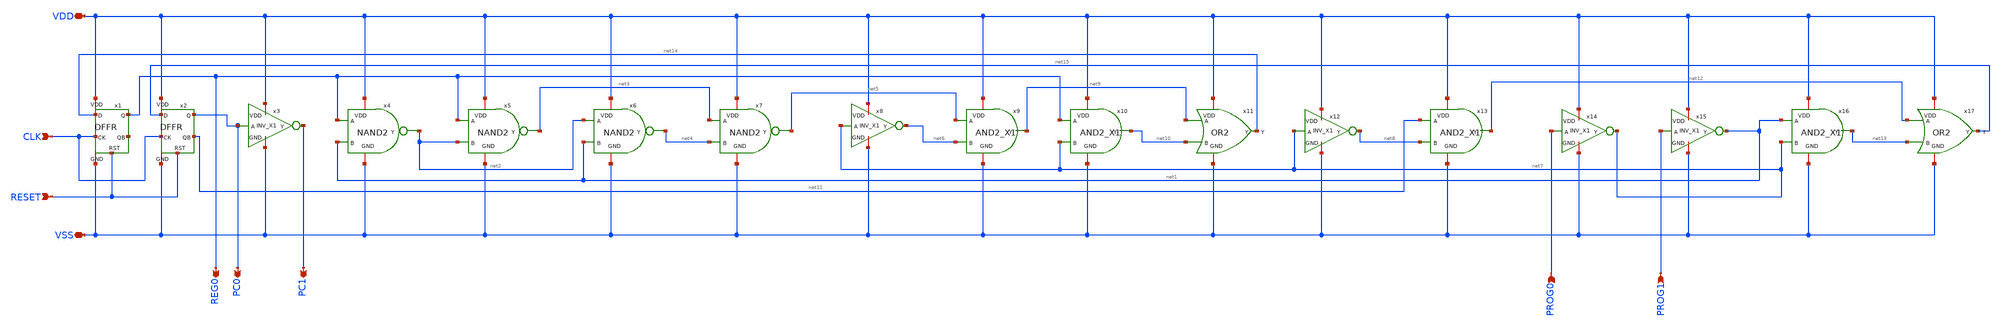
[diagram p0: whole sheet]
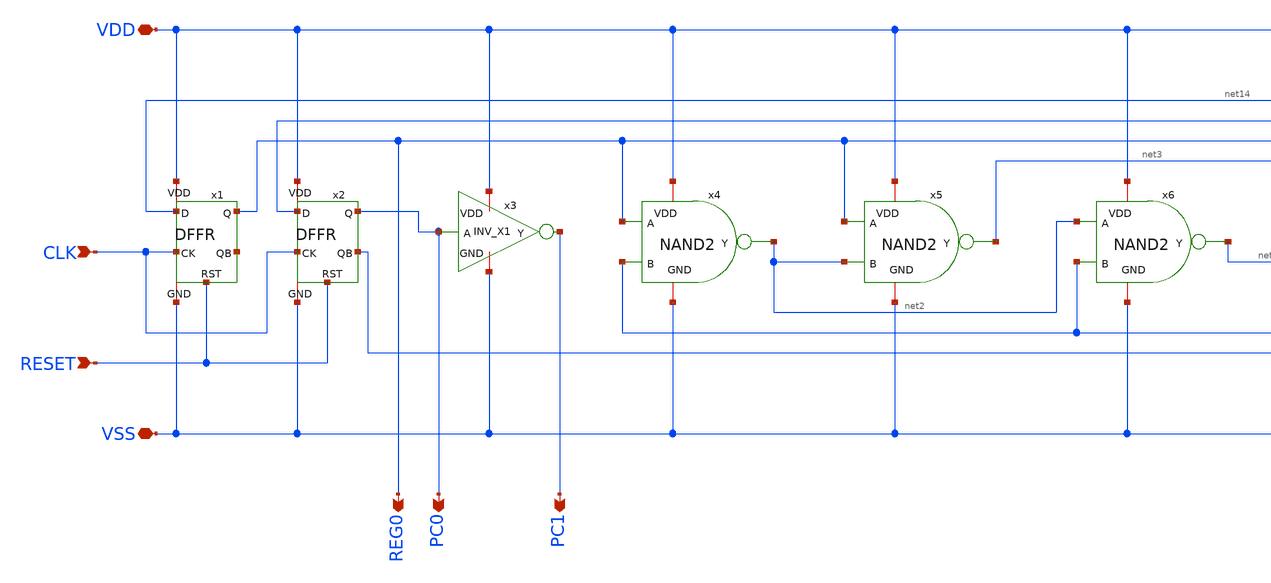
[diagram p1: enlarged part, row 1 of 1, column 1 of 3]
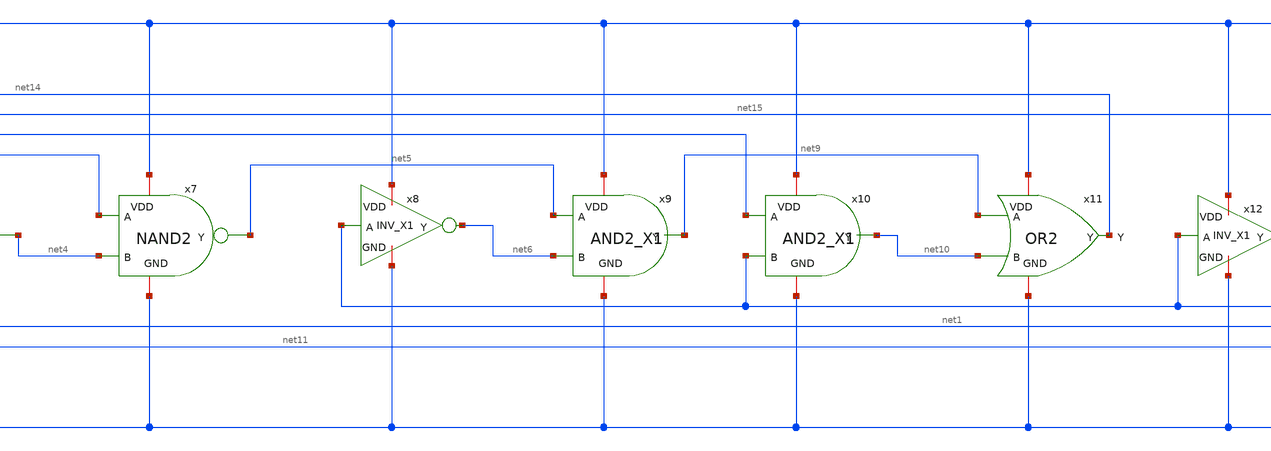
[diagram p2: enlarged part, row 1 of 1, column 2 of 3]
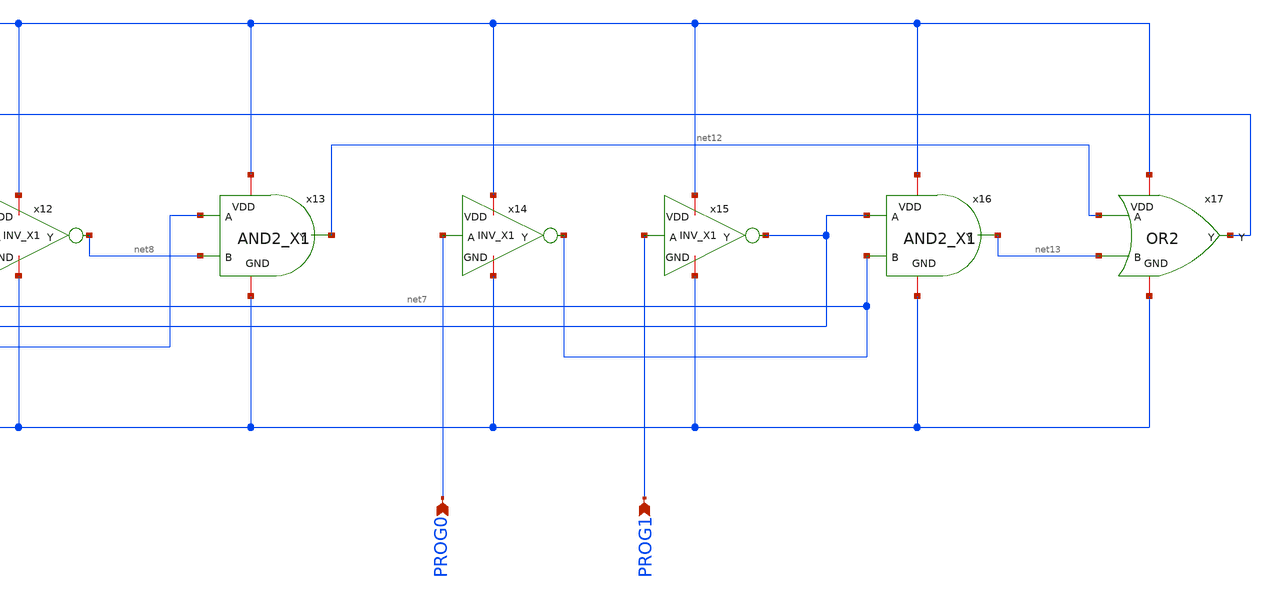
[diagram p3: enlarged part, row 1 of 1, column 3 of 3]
** sch_path: member_project/1bit-CPU_ALL/1bit-CPU_MUX_kyushu/1bit-CPU_1line_sadakata.sch
**.subckt 1bit-CPU_1line_sadakata VDD VSS CLK RESET REG0 PROG1 PROG0 PC0 PC1
*.iopin VDD
*.iopin VSS
*.ipin CLK
*.ipin RESET
*.opin REG0
*.ipin PROG1
*.ipin PROG0
*.opin PC0
*.opin PC1
x1 VDD net16 net14 REG0 RESET VSS CLK DFFR
x2 VDD net11 net15 PC0 RESET VSS CLK DFFR
x3 VDD PC0 PC1 VSS INV_X1
x4 VDD net2 REG0 net1 VSS NAND2
x5 VDD net3 REG0 net2 VSS NAND2
x6 VDD net4 net2 net1 VSS NAND2
x7 VDD net5 net3 net4 VSS NAND2
x8 VDD net7 net6 VSS INV_X1
x9 VDD net9 net5 net6 VSS AND2_X1
x10 VDD net10 REG0 net7 VSS AND2_X1
x11 VDD net14 net9 net10 VSS OR2
x12 VDD net7 net8 VSS INV_X1
x13 VDD net12 net11 net8 VSS AND2_X1
x14 VDD PROG0 net7 VSS INV_X1
x15 VDD PROG1 net1 VSS INV_X1
x16 VDD net13 net1 net7 VSS AND2_X1
x17 VDD net15 net12 net13 VSS OR2
**.ends

* expanding   symbol:  IP62_5_stdcell/DFFR.sym # of pins=7
** sym_path: IP62_5_stdcell/DFFR.sym
** sch_path: IP62_5_stdcell/DFFR.sch
.subckt DFFR VDD QB D Q RST GND CK
*.iopin VDD
*.iopin GND
*.ipin CK
*.ipin D
*.opin Q
*.opin QB
*.ipin RST
XM2 net2 D VDD VDD PMOS w=10.2u l=1u as=0 ad=0 ps=0 pd=0 nrd=0 nrs=0 m=1
XM1 net3 CLK net2 VDD PMOS w=10.2u l=1u as=0 ad=0 ps=0 pd=0 nrd=0 nrs=0 m=1
XM11 net5 net8 VDD VDD PMOS w=10.2u l=1u as=0 ad=0 ps=0 pd=0 nrd=0 nrs=0 m=1
XM12 net3 CKB net5 VDD PMOS w=10.2u l=1u as=0 ad=0 ps=0 pd=0 nrd=0 nrs=0 m=1
XM15 net7 net3 VDD VDD PMOS w=10.2u l=1u as=0 ad=0 ps=0 pd=0 nrd=0 nrs=0 m=1
XM16 net8 RST net7 VDD PMOS w=10.2u l=1u as=0 ad=0 ps=0 pd=0 nrd=0 nrs=0 m=1
XM18 net9 net8 VDD VDD PMOS w=10.2u l=1u as=0 ad=0 ps=0 pd=0 nrd=0 nrs=0 m=1
XM19 net10 CKB net9 VDD PMOS w=10.2u l=1u as=0 ad=0 ps=0 pd=0 nrd=0 nrs=0 m=1
XM23 net12 net14 VDD VDD PMOS w=10.2u l=1u as=0 ad=0 ps=0 pd=0 nrd=0 nrs=0 m=1
XM24 net10 CLK net12 VDD PMOS w=10.2u l=1u as=0 ad=0 ps=0 pd=0 nrd=0 nrs=0 m=1
XM27 net15 net10 VDD VDD PMOS w=10.2u l=1u as=0 ad=0 ps=0 pd=0 nrd=0 nrs=0 m=1
XM28 net14 RST net15 VDD PMOS w=10.2u l=1u as=0 ad=0 ps=0 pd=0 nrd=0 nrs=0 m=1
XM31 QB net14 VDD VDD PMOS w=10.2u l=1u as=0 ad=0 ps=0 pd=0 nrd=0 nrs=0 m=1
XM33 Q QB VDD VDD PMOS w=10.2u l=1u as=0 ad=0 ps=0 pd=0 nrd=0 nrs=0 m=1
XM35 QB net14 GND GND NMOS w=3.4u l=1u as=0 ad=0 ps=0 pd=0 nrd=0 nrs=0 m=1
XM32 Q QB GND GND NMOS w=3.4u l=1u as=0 ad=0 ps=0 pd=0 nrd=0 nrs=0 m=1
XM29 net14 RST GND GND NMOS w=3.4u l=1u as=0 ad=0 ps=0 pd=0 nrd=0 nrs=0 m=1
XM30 net14 net10 GND GND NMOS w=3.4u l=1u as=0 ad=0 ps=0 pd=0 nrd=0 nrs=0 m=1
XM25 net10 CKB net13 GND NMOS w=3.4u l=1u as=0 ad=0 ps=0 pd=0 nrd=0 nrs=0 m=1
XM26 net13 net14 GND GND NMOS w=3.4u l=1u as=0 ad=0 ps=0 pd=0 nrd=0 nrs=0 m=1
XM20 net10 CLK net11 GND NMOS w=3.4u l=1u as=0 ad=0 ps=0 pd=0 nrd=0 nrs=0 m=1
XM21 net11 net8 GND GND NMOS w=3.4u l=1u as=0 ad=0 ps=0 pd=0 nrd=0 nrs=0 m=1
XM17 net8 net3 GND GND NMOS w=3.4u l=1u as=0 ad=0 ps=0 pd=0 nrd=0 nrs=0 m=1
XM22 net8 RST GND GND NMOS w=3.4u l=1u as=0 ad=0 ps=0 pd=0 nrd=0 nrs=0 m=1
XM13 net3 CLK net6 GND NMOS w=3.4u l=1u as=0 ad=0 ps=0 pd=0 nrd=0 nrs=0 m=1
XM14 net6 net8 GND GND NMOS w=3.4u l=1u as=0 ad=0 ps=0 pd=0 nrd=0 nrs=0 m=1
XM7 net3 CKB net4 GND NMOS w=3.4u l=1u as=0 ad=0 ps=0 pd=0 nrd=0 nrs=0 m=1
XM8 net4 D GND GND NMOS w=3.4u l=1u as=0 ad=0 ps=0 pd=0 nrd=0 nrs=0 m=1
XM3 net1 CK VDD VDD PMOS w=10.2u l=1u as=0 ad=0 ps=0 pd=0 nrd=0 nrs=0 m=1
XM4 CLK net1 VDD VDD PMOS w=10.2u l=1u as=0 ad=0 ps=0 pd=0 nrd=0 nrs=0 m=1
XM5 CKB CLK VDD VDD PMOS w=10.2u l=1u as=0 ad=0 ps=0 pd=0 nrd=0 nrs=0 m=1
XM34 net1 CK GND GND NMOS w=3.4u l=1u as=0 ad=0 ps=0 pd=0 nrd=0 nrs=0 m=1
XM6 CLK net1 GND GND NMOS w=3.4u l=1u as=0 ad=0 ps=0 pd=0 nrd=0 nrs=0 m=1
XM9 CKB CLK GND GND NMOS w=3.4u l=1u as=0 ad=0 ps=0 pd=0 nrd=0 nrs=0 m=1
.ends


* expanding   symbol:  IP62_5_stdcell/INV_X1.sym # of pins=4
** sym_path: IP62_5_stdcell/INV_X1.sym
** sch_path: IP62_5_stdcell/INV_X1.sch
.subckt INV_X1 VDD A Y GND
*.ipin A
*.opin Y
*.iopin GND
*.iopin VDD
XM7 Y A VDD VDD PMOS w=10.2u l=1u as=0 ad=0 ps=0 pd=0 nrd=0 nrs=0 m=1
XM2 Y A GND GND NMOS w=3.4u l=1u as=0 ad=0 ps=0 pd=0 nrd=0 nrs=0 m=1
.ends


* expanding   symbol:  IP62_5_stdcell/NAND2.sym # of pins=5
** sym_path: IP62_5_stdcell/NAND2.sym
** sch_path: IP62_5_stdcell/NAND2.sch
.subckt NAND2 VDD Y A B GND
*.ipin B
*.ipin A
*.opin Y
*.iopin GND
*.iopin VDD
XM7 Y A VDD VDD PMOS w=10.2u l=1u as=0 ad=0 ps=0 pd=0 nrd=0 nrs=0 m=1
XM1 Y B VDD VDD PMOS w=10.2u l=1u as=0 ad=0 ps=0 pd=0 nrd=0 nrs=0 m=1
XM2 Y B net1 GND NMOS w=3.4u l=1u as=0 ad=0 ps=0 pd=0 nrd=0 nrs=0 m=1
XM3 net1 A GND GND NMOS w=3.4u l=1u as=0 ad=0 ps=0 pd=0 nrd=0 nrs=0 m=1
.ends


* expanding   symbol:  IP62_5_stdcell/AND2_X1.sym # of pins=5
** sym_path: IP62_5_stdcell/AND2_X1.sym
** sch_path: IP62_5_stdcell/AND2_X1.sch
.subckt AND2_X1 VDD Y A B GND
*.opin Y
*.ipin A
*.ipin B
*.iopin VDD
*.iopin GND
XM7 net1 B VDD VDD PMOS w=10.2u l=1u as=0 ad=0 ps=0 pd=0 nrd=0 nrs=0 m=1
XM1 net1 A VDD VDD PMOS w=10.2u l=1u as=0 ad=0 ps=0 pd=0 nrd=0 nrs=0 m=1
XM2 Y net1 VDD VDD PMOS w=10.2u l=1u as=0 ad=0 ps=0 pd=0 nrd=0 nrs=0 m=1
XM3 Y net1 GND GND NMOS w=3.4u l=1u as=0 ad=0 ps=0 pd=0 nrd=0 nrs=0 m=1
XM4 net1 A net2 GND NMOS w=3.4u l=1u as=0 ad=0 ps=0 pd=0 nrd=0 nrs=0 m=1
XM5 net2 B GND GND NMOS w=3.4u l=1u as=0 ad=0 ps=0 pd=0 nrd=0 nrs=0 m=1
.ends


* expanding   symbol:  IP62_5_stdcell/OR2.sym # of pins=5
** sym_path: IP62_5_stdcell/OR2.sym
** sch_path: IP62_5_stdcell/OR2.sch
.subckt OR2 VDD Y A B GND
*.ipin A
*.ipin B
*.opin Y
*.iopin VDD
*.iopin GND
XM7 net2 B VDD VDD PMOS w=10.2u l=1u as=0 ad=0 ps=0 pd=0 nrd=0 nrs=0 m=1
XM2 net1 A net2 VDD PMOS w=10.2u l=1u as=0 ad=0 ps=0 pd=0 nrd=0 nrs=0 m=1
XM4 Y net1 VDD VDD PMOS w=10.2u l=1u as=0 ad=0 ps=0 pd=0 nrd=0 nrs=0 m=1
XM1 net1 B GND GND NMOS w=3.4u l=1u as=0 ad=0 ps=0 pd=0 nrd=0 nrs=0 m=1
XM3 net1 A GND GND NMOS w=3.4u l=1u as=0 ad=0 ps=0 pd=0 nrd=0 nrs=0 m=1
XM5 Y net1 GND GND NMOS w=3.4u l=1u as=0 ad=0 ps=0 pd=0 nrd=0 nrs=0 m=1
.ends

.end
